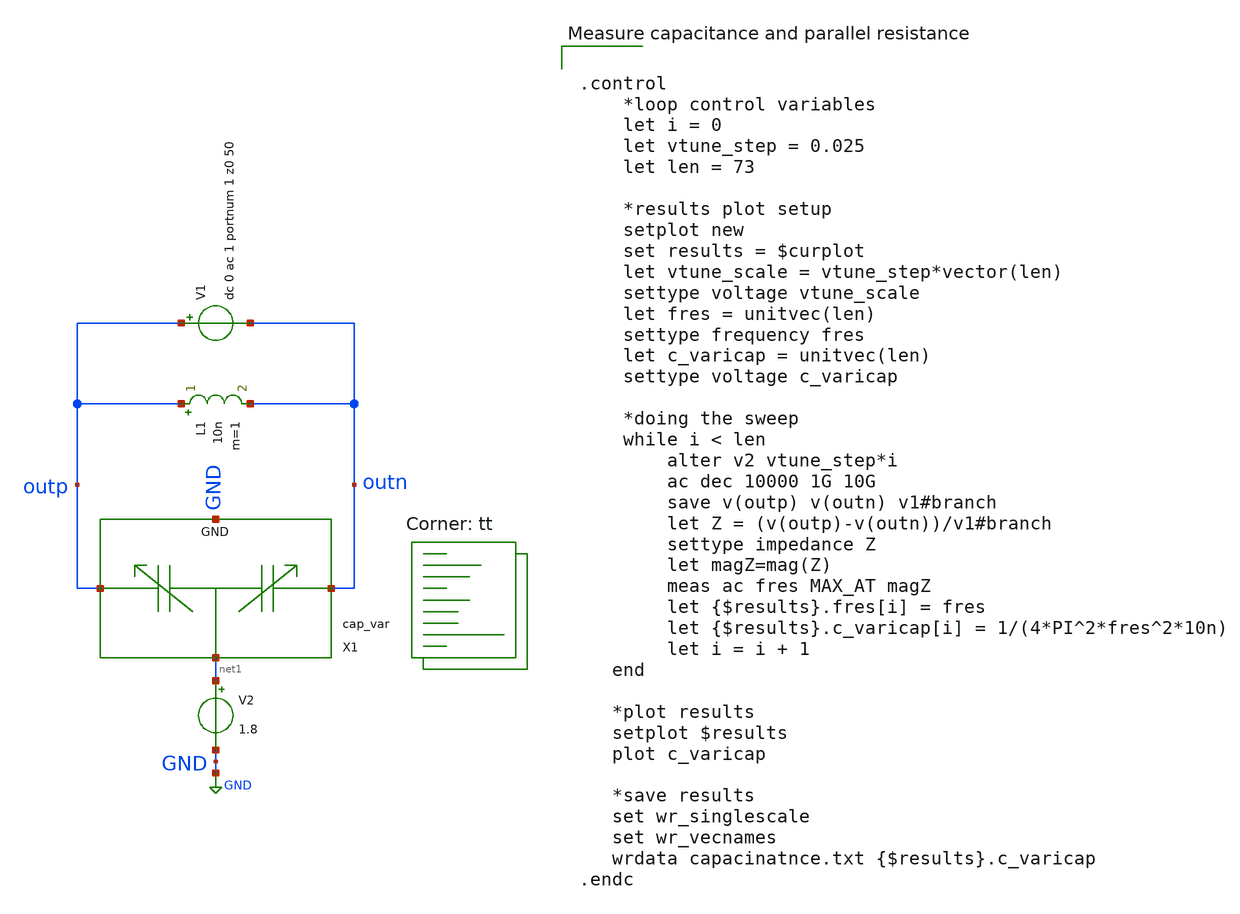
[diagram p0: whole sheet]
** sch_path: xschem/vco/testbenches/varicap/varicap_capacity_measurement_tb.sch
**.subckt varicap_capacity_measurement_tb
X1 outp outn GND net1 cap_var
L1 outp outn 10n m=1
V1 outp outn dc 0 ac 1 portnum 1 z0 50
V2 net1 GND 1.8
**** begin user architecture code
.lib $::SKYWATER_MODELS/sky130.lib.spice tt


.control
    *loop control variables
    let i = 0
    let vtune_step = 0.025
    let len = 73

    *results plot setup
    setplot new
    set results = $curplot
    let vtune_scale = vtune_step*vector(len)
    settype voltage vtune_scale
    let fres = unitvec(len)
    settype frequency fres
    let c_varicap = unitvec(len)
    settype voltage c_varicap

    *doing the sweep
    while i < len
        alter v2 vtune_step*i
        ac dec 10000 1G 10G
        save v(outp) v(outn) v1#branch
        let Z = (v(outp)-v(outn))/v1#branch
        settype impedance Z
        let magZ=mag(Z)
        meas ac fres MAX_AT magZ
        let {$results}.fres[i] = fres
        let {$results}.c_varicap[i] = 1/(4*PI^2*fres^2*10n)
        let i = i + 1
   end

   *plot results
   setplot $results
   plot c_varicap

   *save results
   set wr_singlescale
   set wr_vecnames
   wrdata capacinatnce.txt {$results}.c_varicap
.endc


**** end user architecture code
**.ends

* expanding   symbol:  vco/parts/cap_var.sym # of pins=4
** sym_path: xschem/vco/parts/cap_var.sym
** sch_path: xschem/vco/parts/cap_var.sch
.subckt cap_var OUT_P OUT_N GND Vtune
*.iopin OUT_P
*.iopin OUT_N
*.iopin GND
*.ipin Vtune
XC1 OUT_P Vtune GND sky130_fd_pr__cap_var_lvt W=4 L=0.6 VM=14 m=14
XC2 OUT_N Vtune GND sky130_fd_pr__cap_var_lvt W=4 L=0.6 VM=14 m=14
.ends

.GLOBAL GND
.end
